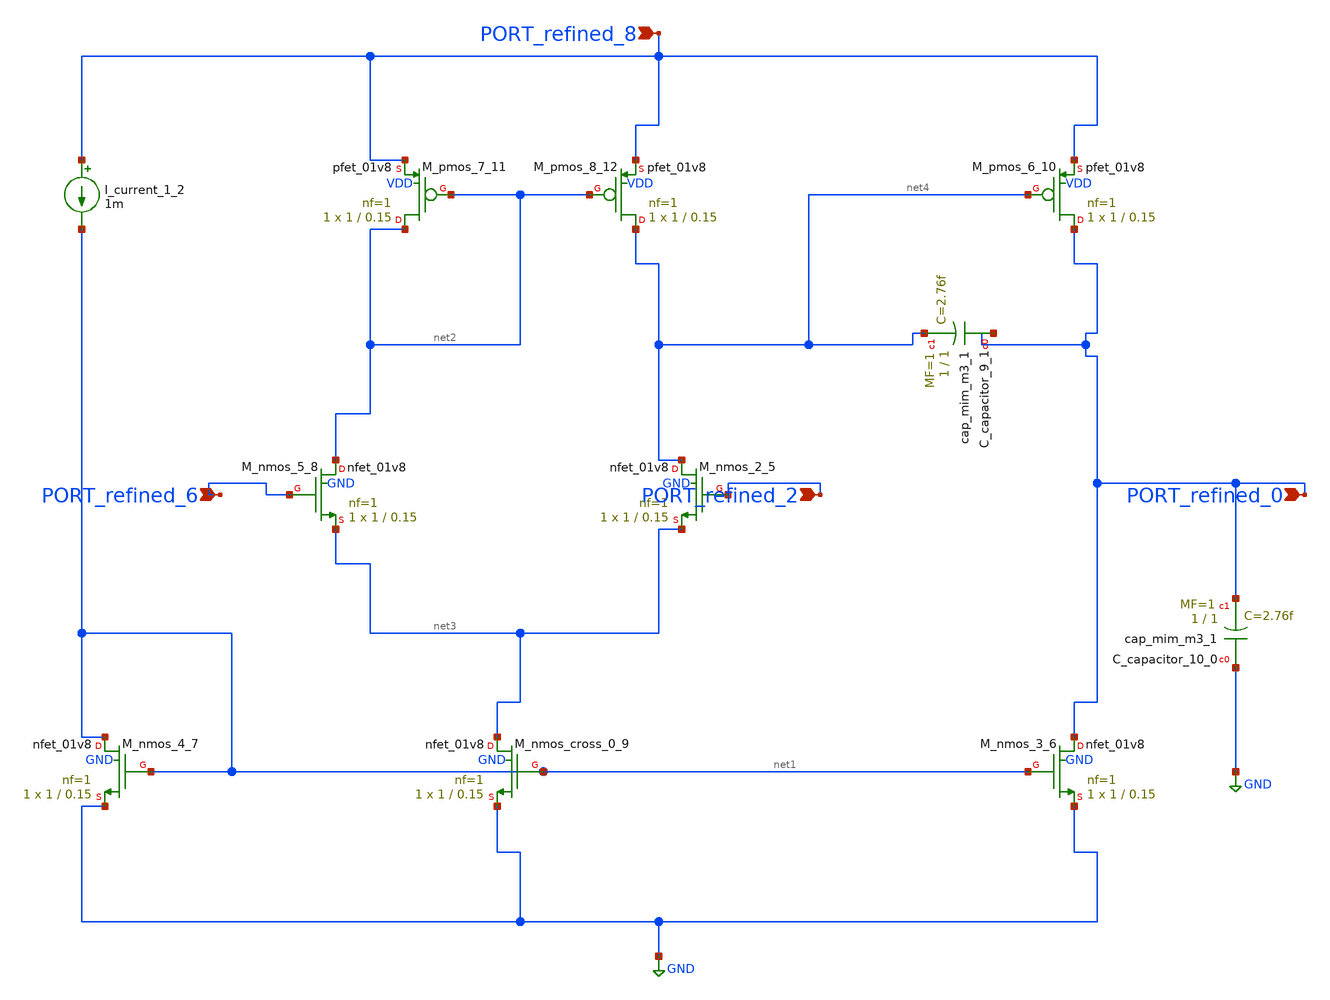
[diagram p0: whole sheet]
** sch_path: schematics/Image2Net/053.sch
**.subckt 053 PORT_refined_2 PORT_refined_0 PORT_refined_6 PORT_refined_8
*.ipin PORT_refined_2
*.ipin PORT_refined_0
*.ipin PORT_refined_6
*.ipin PORT_refined_8
XC_capacitor_10_0 GND PORT_refined_0 sky130_fd_pr__cap_mim_m3_1 W=1 L=1 MF=1 m=1
XC_capacitor_9_1 PORT_refined_0 net4 sky130_fd_pr__cap_mim_m3_1 W=1 L=1 MF=1 m=1
I_current_1_2 PORT_refined_8 net1 1m
XM_nmos_2_5 net4 PORT_refined_2 net3 GND sky130_fd_pr__nfet_01v8 L=0.15 W=1 nf=1 ad='int((1 + 1)/2) * 1 / 1 * 0.29'
+ as='int((1 + 2)/2) * 1 / 1 * 0.29' pd='2*int((1 + 1)/2) * (1 / 1 + 0.29)' ps='2*int((1 + 2)/2) * (1 / 1 + 0.29)'
+ nrd='0.29 / 1 ' nrs='0.29 / 1 ' sa=0 sb=0 sd=0 mult=1 m=1
XM_nmos_3_6 PORT_refined_0 net1 GND GND sky130_fd_pr__nfet_01v8 L=0.15 W=1 nf=1 ad='int((1 + 1)/2) * 1 / 1 * 0.29'
+ as='int((1 + 2)/2) * 1 / 1 * 0.29' pd='2*int((1 + 1)/2) * (1 / 1 + 0.29)' ps='2*int((1 + 2)/2) * (1 / 1 + 0.29)'
+ nrd='0.29 / 1 ' nrs='0.29 / 1 ' sa=0 sb=0 sd=0 mult=1 m=1
XM_nmos_4_7 net1 net1 GND GND sky130_fd_pr__nfet_01v8 L=0.15 W=1 nf=1 ad='int((1 + 1)/2) * 1 / 1 * 0.29'
+ as='int((1 + 2)/2) * 1 / 1 * 0.29' pd='2*int((1 + 1)/2) * (1 / 1 + 0.29)' ps='2*int((1 + 2)/2) * (1 / 1 + 0.29)'
+ nrd='0.29 / 1 ' nrs='0.29 / 1 ' sa=0 sb=0 sd=0 mult=1 m=1
XM_nmos_5_8 net2 PORT_refined_6 net3 GND sky130_fd_pr__nfet_01v8 L=0.15 W=1 nf=1 ad='int((1 + 1)/2) * 1 / 1 * 0.29'
+ as='int((1 + 2)/2) * 1 / 1 * 0.29' pd='2*int((1 + 1)/2) * (1 / 1 + 0.29)' ps='2*int((1 + 2)/2) * (1 / 1 + 0.29)'
+ nrd='0.29 / 1 ' nrs='0.29 / 1 ' sa=0 sb=0 sd=0 mult=1 m=1
XM_nmos_cross_0_9 net3 net1 GND GND sky130_fd_pr__nfet_01v8 L=0.15 W=1 nf=1 ad='int((1 + 1)/2) * 1 / 1 * 0.29'
+ as='int((1 + 2)/2) * 1 / 1 * 0.29' pd='2*int((1 + 1)/2) * (1 / 1 + 0.29)' ps='2*int((1 + 2)/2) * (1 / 1 + 0.29)'
+ nrd='0.29 / 1 ' nrs='0.29 / 1 ' sa=0 sb=0 sd=0 mult=1 m=1
XM_pmos_6_10 PORT_refined_0 net4 PORT_refined_8 VDD sky130_fd_pr__pfet_01v8 L=0.15 W=1 nf=1 ad='int((1 + 1)/2) * 1 / 1 * 0.29'
+ as='int((1 + 2)/2) * 1 / 1 * 0.29' pd='2*int((1 + 1)/2) * (1 / 1 + 0.29)' ps='2*int((1 + 2)/2) * (1 / 1 + 0.29)'
+ nrd='0.29 / 1 ' nrs='0.29 / 1 ' sa=0 sb=0 sd=0 mult=1 m=1
XM_pmos_7_11 net2 net2 PORT_refined_8 VDD sky130_fd_pr__pfet_01v8 L=0.15 W=1 nf=1 ad='int((1 + 1)/2) * 1 / 1 * 0.29'
+ as='int((1 + 2)/2) * 1 / 1 * 0.29' pd='2*int((1 + 1)/2) * (1 / 1 + 0.29)' ps='2*int((1 + 2)/2) * (1 / 1 + 0.29)'
+ nrd='0.29 / 1 ' nrs='0.29 / 1 ' sa=0 sb=0 sd=0 mult=1 m=1
XM_pmos_8_12 net4 net2 PORT_refined_8 VDD sky130_fd_pr__pfet_01v8 L=0.15 W=1 nf=1 ad='int((1 + 1)/2) * 1 / 1 * 0.29'
+ as='int((1 + 2)/2) * 1 / 1 * 0.29' pd='2*int((1 + 1)/2) * (1 / 1 + 0.29)' ps='2*int((1 + 2)/2) * (1 / 1 + 0.29)'
+ nrd='0.29 / 1 ' nrs='0.29 / 1 ' sa=0 sb=0 sd=0 mult=1 m=1
**.ends
.GLOBAL GND
.end
